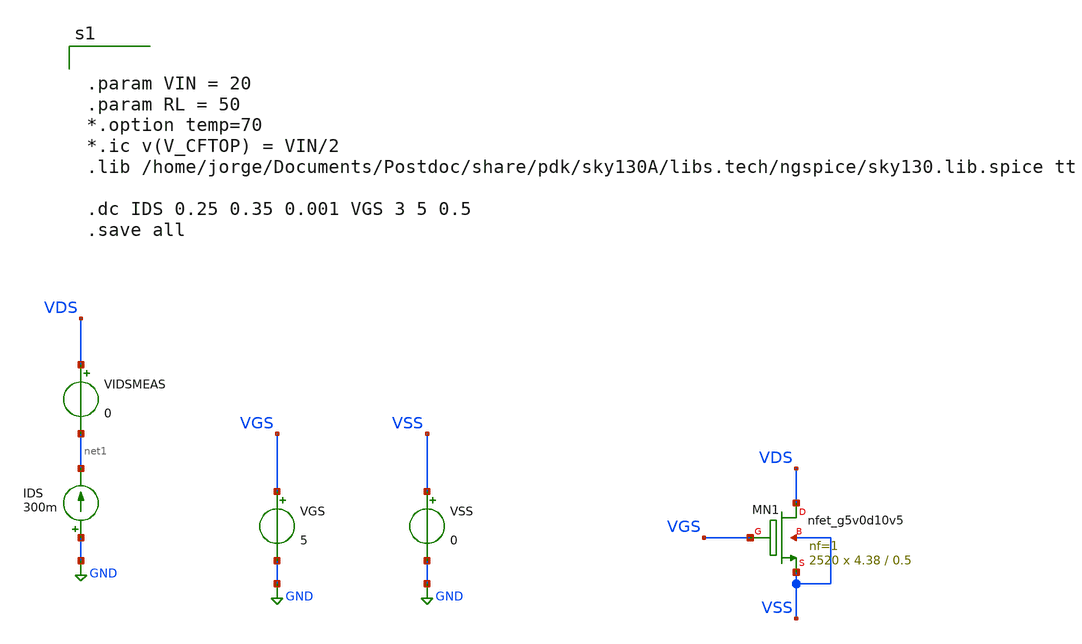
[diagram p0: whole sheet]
** sch_path: xschem/dev_switches/NMOS_allfingers_RONcalc_v2p1_20220614.sch
**.subckt NMOS_allfingers_RONcalc_v2p1_20220614
XMN1 VDS VGS VSS VSS sky130_fd_pr__nfet_g5v0d10v5 L=0.5 W=4.38 nf=1 ad='int((nf+1)/2) * W/nf * 0.29'
+ as='int((nf+2)/2) * W/nf * 0.29' pd='2*int((nf+1)/2) * (W/nf + 0.29)' ps='2*int((nf+2)/2) * (W/nf + 0.29)'
+ nrd='0.29 / W' nrs='0.29 / W' sa=0 sb=0 sd=0 mult=2520 m=2520
VGS VGS GND 5
VSS VSS GND 0
IDS GND net1 300m
VIDSMEAS VDS net1 0
**** begin user architecture code


.param VIN = 20
.param RL = 50
*.option temp=70
*.ic v(V_CFTOP) = VIN/2
.lib /home/jorge/Documents/Postdoc/share/pdk/sky130A/libs.tech/ngspice/sky130.lib.spice tt

.dc IDS 0.25 0.35 0.001 VGS 3 5 0.5
.save all


**** end user architecture code
**.ends
.GLOBAL GND
.end
